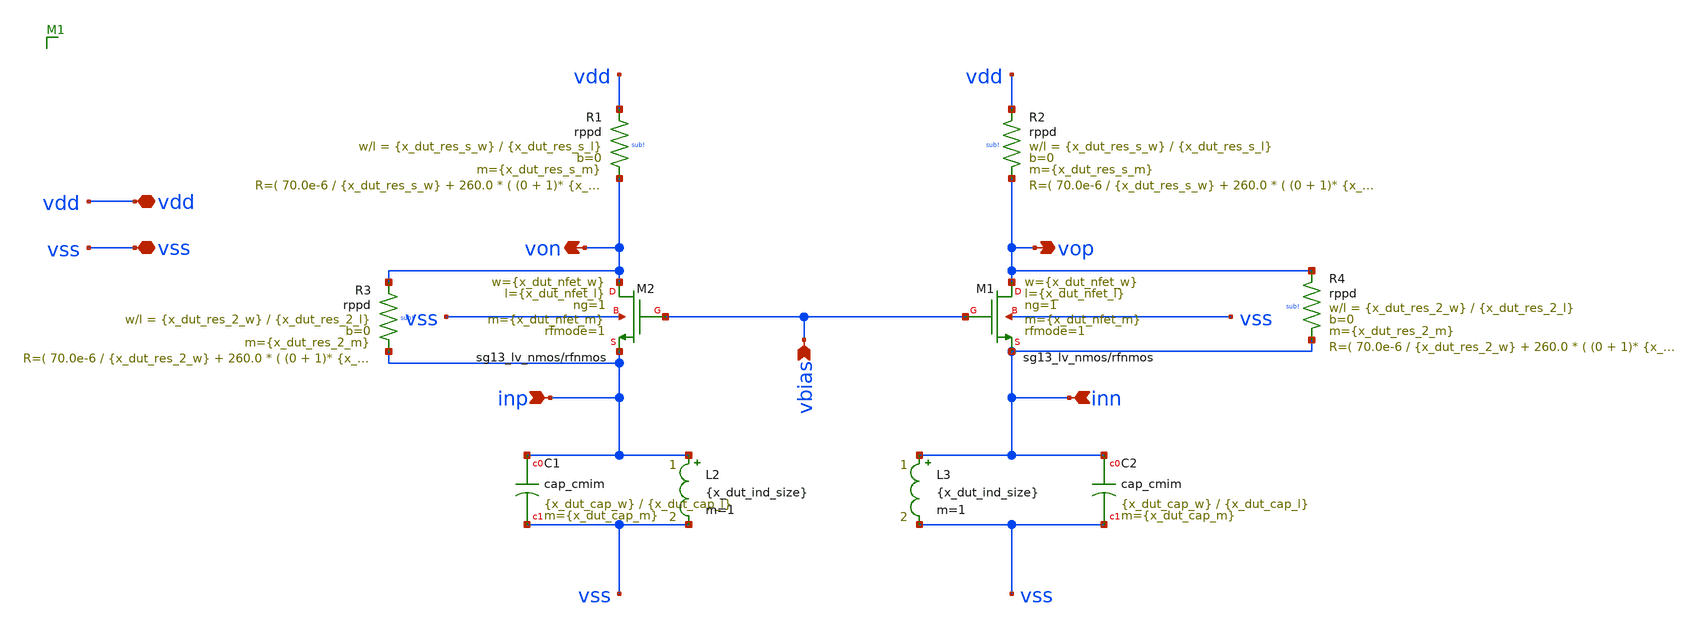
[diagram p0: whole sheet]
** sch_path: examples/tunable-tia/ihp-sg13g2/xschem/tia-topo-2/tia-bpf-2-ideal-ind.sch
**.subckt tia-bpf-2-ideal-ind vdd vss inp inn von vop vbias
*.iopin vdd
*.iopin vss
*.ipin inp
*.ipin inn
*.opin von
*.opin vop
*.ipin vbias
XM1 vop vbias inn vss sg13_lv_nmos w={x_dut_nfet_w} l={x_dut_nfet_l} ng=1 m={x_dut_nfet_m} rfmode=1 mm_ok=1
XM2 von vbias inp vss sg13_lv_nmos w={x_dut_nfet_w} l={x_dut_nfet_l} ng=1 m={x_dut_nfet_m} rfmode=1 mm_ok=1
XC1 inp vss cap_cmim w={x_dut_cap_w} l={x_dut_cap_l} m={x_dut_cap_m} mm_ok=1
XC2 inn vss cap_cmim w={x_dut_cap_w} l={x_dut_cap_l} m={x_dut_cap_m} mm_ok=1
XR1 vdd von sub! rppd w={x_dut_res_s_w} l={x_dut_res_s_l} m={x_dut_res_s_m} b=0 mm_ok=1
XR2 vdd vop sub! rppd w={x_dut_res_s_w} l={x_dut_res_s_l} m={x_dut_res_s_m} b=0 mm_ok=1
XR3 von inp sub! rppd w={x_dut_res_2_w} l={x_dut_res_2_l} m={x_dut_res_2_m} b=0 mm_ok=1
L2 inp vss {x_dut_ind_size} m=1
L3 inn vss {x_dut_ind_size} m=1
XR4 vop inn sub! rppd w={x_dut_res_2_w} l={x_dut_res_2_l} m={x_dut_res_2_m} b=0 mm_ok=1
**.ends
.end
